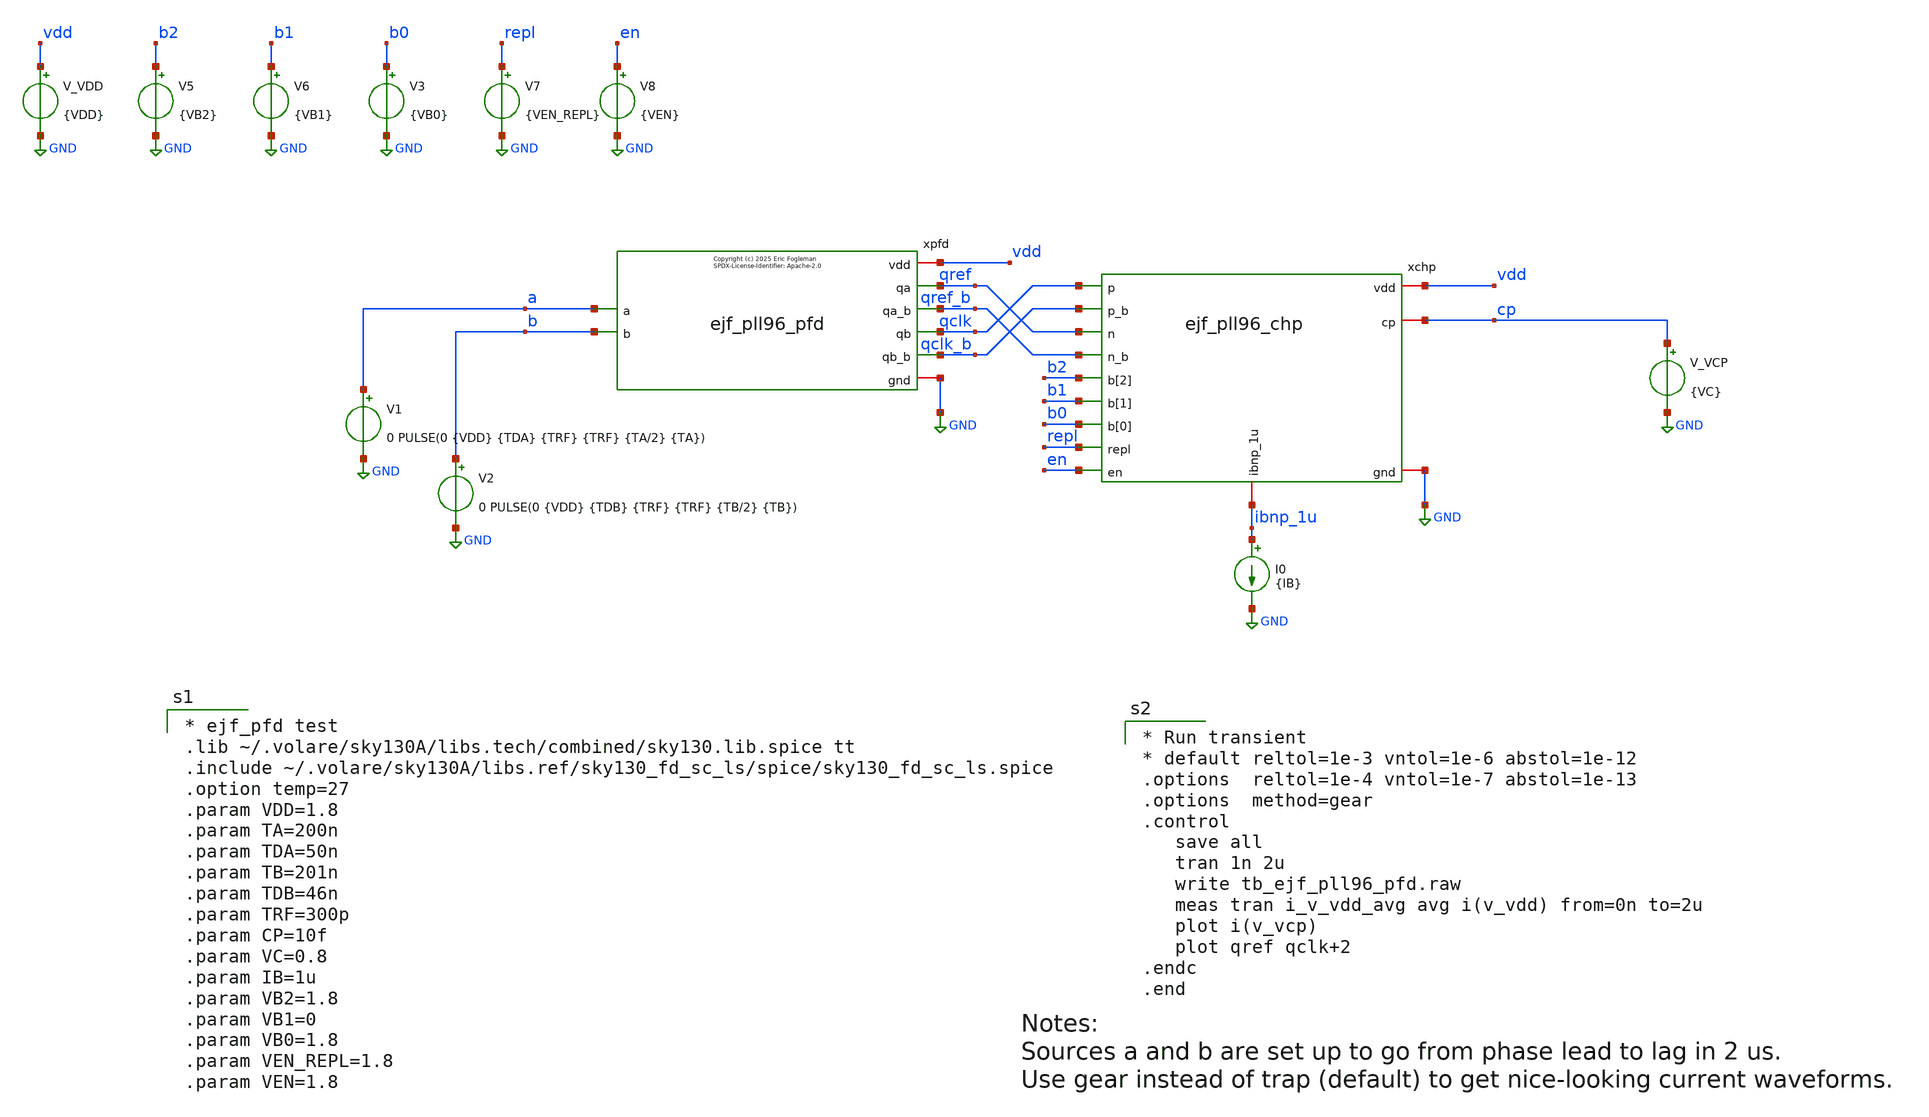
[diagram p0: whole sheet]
** sch_path: xschem/tb_ejf_pll96_pfd.sch
* xschem/ejf_pll96_dbuf.sym:
* Copyright (c) 2025 Eric Fogleman
**.subckt tb_ejf_pll96_pfd
V_VDD vdd GND {VDD}
.save i(v_vdd)
V1 a GND 0 PULSE(0 {VDD} {TDA} {TRF} {TRF} {TA/2} {TA})
xpfd qref a qclk b vdd GND qref_b qclk_b ejf_pll96_pfd
V2 b GND 0 PULSE(0 {VDD} {TDB} {TRF} {TRF} {TB/2} {TB})
xchp vdd qclk ibnp_1u qclk_b cp qref_b qref GND b1 repl en b2 b0 ejf_pll96_chp
I0 ibnp_1u GND {IB}
V_VCP cp GND {VC}
.save i(v_vcp)
V5 b2 GND {VB2}
.save i(v5)
V6 b1 GND {VB1}
.save i(v6)
V7 repl GND {VEN_REPL}
.save i(v7)
V8 en GND {VEN}
.save i(v8)
V3 b0 GND {VB0}
.save i(v3)
**** begin user architecture code

* ejf_pfd test
.lib ~/.volare/sky130A/libs.tech/combined/sky130.lib.spice tt
.include ~/.volare/sky130A/libs.ref/sky130_fd_sc_ls/spice/sky130_fd_sc_ls.spice
.option temp=27
.param VDD=1.8
.param TA=200n
.param TDA=50n
.param TB=201n
.param TDB=46n
.param TRF=300p
.param CP=10f
.param VC=0.8
.param IB=1u
.param VB2=1.8
.param VB1=0
.param VB0=1.8
.param VEN_REPL=1.8
.param VEN=1.8



* Run transient
* default reltol=1e-3 vntol=1e-6 abstol=1e-12
.options  reltol=1e-4 vntol=1e-7 abstol=1e-13
.options  method=gear
.control
   save all
   tran 1n 2u
   write tb_ejf_pll96_pfd.raw
   meas tran i_v_vdd_avg avg i(v_vdd) from=0n to=2u
   plot i(v_vcp)
   plot qref qclk+2
.endc
.end

**** end user architecture code
**.ends

* expanding   symbol:  ejf_pll96_pfd.sym # of pins=8
** sym_path: xschem/ejf_pll96_pfd.sym
** sch_path: xschem/ejf_pll96_pfd.sch
.subckt ejf_pll96_pfd qa a qb b vdd gnd qa_b qb_b
*.iopin vdd
*.iopin gnd
*.ipin a
*.ipin b
*.opin qa
*.opin qb
*.opin qa_b
*.opin qb_b
x3 a_b b_b gnd gnd vdd vdd y_par sky130_fd_sc_ls__nor2_2
x4 net1 gnd gnd vdd vdd rst_b sky130_fd_sc_ls__clkinv_1
x1 a vdd rst_b gnd gnd vdd vdd qa0 sky130_fd_sc_ls__dfrtp_2
x2 b vdd rst_b gnd gnd vdd vdd qb0 sky130_fd_sc_ls__dfrtp_2
x6 vdd qa0 qa_b qa gnd a_b ejf_pll96_diff_buf
x7 vdd qb0 qb_b qb gnd b_b ejf_pll96_diff_buf
x8 b_b a_b gnd gnd vdd vdd y_par sky130_fd_sc_ls__nor2_2
x10 y_par gnd gnd vdd vdd net2 sky130_fd_sc_ls__dlygate4sd3_1
x5 net2 gnd gnd vdd vdd net1 sky130_fd_sc_ls__dlygate4sd3_1
**** begin user architecture code

* Copyright (c) Eric Fogleman 2025
* SPDX-License-Identifier: Apache-2.0

**** end user architecture code
.ends


* expanding   symbol:  ejf_pll96_chp.sym # of pins=13
** sym_path: xschem/ejf_pll96_chp.sym
** sch_path: xschem/ejf_pll96_chp.sch
.subckt ejf_pll96_chp vdd p ibnp_1u p_b cp n_b n gnd b[1] repl en b[2] b[0]
*.iopin vdd
*.iopin gnd
*.iopin ibnp_1u
*.iopin cp
*.ipin p
*.ipin n_b
*.ipin p_b
*.ipin n
*.ipin en
*.ipin b[2],b[1],b[0]
*.ipin repl
XMP2_2 mp2d net12 vdd vdd sky130_fd_pr__pfet_01v8_lvt L=1.2 W=1.2 nf=2 ad='int((nf+1)/2) * W/nf * 0.29'
+ as='int((nf+2)/2) * W/nf * 0.29' pd='2*int((nf+1)/2) * (W/nf + 0.29)' ps='2*int((nf+2)/2) * (W/nf + 0.29)'
+ nrd='0.29 / W' nrs='0.29 / W' sa=0 sb=0 sd=0 mult=1 m=1
XMN2 net1 mn1g gnd gnd sky130_fd_pr__nfet_01v8 L=1.2 W=0.6 nf=1 ad='int((nf+1)/2) * W/nf * 0.29' as='int((nf+2)/2) * W/nf * 0.29'
+ pd='2*int((nf+1)/2) * (W/nf + 0.29)' ps='2*int((nf+2)/2) * (W/nf + 0.29)' nrd='0.29 / W' nrs='0.29 / W'
+ sa=0 sb=0 sd=0 mult=1 m=1
XMN2C mn1g mn1cg net1 gnd sky130_fd_pr__nfet_01v8 L=0.3 W=0.6 nf=1 ad='int((nf+1)/2) * W/nf * 0.29' as='int((nf+2)/2) * W/nf * 0.29'
+ pd='2*int((nf+1)/2) * (W/nf + 0.29)' ps='2*int((nf+2)/2) * (W/nf + 0.29)' nrd='0.29 / W' nrs='0.29 / W'
+ sa=0 sb=0 sd=0 mult=1 m=1
XMP1 mp1d mp1g vdd vdd sky130_fd_pr__pfet_01v8_lvt L=1.2 W=1.8 nf=3 ad='int((nf+1)/2) * W/nf * 0.29'
+ as='int((nf+2)/2) * W/nf * 0.29' pd='2*int((nf+1)/2) * (W/nf + 0.29)' ps='2*int((nf+2)/2) * (W/nf + 0.29)'
+ nrd='0.29 / W' nrs='0.29 / W' sa=0 sb=0 sd=0 mult=5 m=5
XMP2C mp1g ibnp_1u mp2d vdd sky130_fd_pr__pfet_01v8_lvt L=0.35 W=1.2 nf=1 ad='int((nf+1)/2) * W/nf * 0.29'
+ as='int((nf+2)/2) * W/nf * 0.29' pd='2*int((nf+1)/2) * (W/nf + 0.29)' ps='2*int((nf+2)/2) * (W/nf + 0.29)'
+ nrd='0.29 / W' nrs='0.29 / W' sa=0 sb=0 sd=0 mult=1 m=1
XMP1C mp1cd ibnp_1u mp1d vdd sky130_fd_pr__pfet_01v8_lvt L=0.35 W=1.2 nf=1 ad='int((nf+1)/2) * W/nf * 0.29'
+ as='int((nf+2)/2) * W/nf * 0.29' pd='2*int((nf+1)/2) * (W/nf + 0.29)' ps='2*int((nf+2)/2) * (W/nf + 0.29)'
+ nrd='0.29 / W' nrs='0.29 / W' sa=0 sb=0 sd=0 mult=5 m=5
XMN1 mn1d mn1g gnd gnd sky130_fd_pr__nfet_01v8 L=1.2 W=0.6 nf=1 ad='int((nf+1)/2) * W/nf * 0.29' as='int((nf+2)/2) * W/nf * 0.29'
+ pd='2*int((nf+1)/2) * (W/nf + 0.29)' ps='2*int((nf+2)/2) * (W/nf + 0.29)' nrd='0.29 / W' nrs='0.29 / W'
+ sa=0 sb=0 sd=0 mult=5 m=5
XM1C mn1cd mn1cg mn1d gnd sky130_fd_pr__nfet_01v8 L=0.3 W=0.6 nf=1 ad='int((nf+1)/2) * W/nf * 0.29' as='int((nf+2)/2) * W/nf * 0.29'
+ pd='2*int((nf+1)/2) * (W/nf + 0.29)' ps='2*int((nf+2)/2) * (W/nf + 0.29)' nrd='0.29 / W' nrs='0.29 / W'
+ sa=0 sb=0 sd=0 mult=5 m=5
XMP11 cp_repl p mp1cd vdd sky130_fd_pr__pfet_01v8 L=0.15 W=1 nf=1 ad='int((nf+1)/2) * W/nf * 0.29' as='int((nf+2)/2) * W/nf * 0.29'
+ pd='2*int((nf+1)/2) * (W/nf + 0.29)' ps='2*int((nf+2)/2) * (W/nf + 0.29)' nrd='0.29 / W' nrs='0.29 / W'
+ sa=0 sb=0 sd=0 mult=1 m=1
XMN11 cp_repl n_b mn1cd gnd sky130_fd_pr__nfet_01v8 L=0.15 W=1 nf=1 ad='int((nf+1)/2) * W/nf * 0.29'
+ as='int((nf+2)/2) * W/nf * 0.29' pd='2*int((nf+1)/2) * (W/nf + 0.29)' ps='2*int((nf+2)/2) * (W/nf + 0.29)'
+ nrd='0.29 / W' nrs='0.29 / W' sa=0 sb=0 sd=0 mult=1 m=1
XMP10 cp p_b mp1cd vdd sky130_fd_pr__pfet_01v8 L=0.15 W=1 nf=1 ad='int((nf+1)/2) * W/nf * 0.29' as='int((nf+2)/2) * W/nf * 0.29'
+ pd='2*int((nf+1)/2) * (W/nf + 0.29)' ps='2*int((nf+2)/2) * (W/nf + 0.29)' nrd='0.29 / W' nrs='0.29 / W'
+ sa=0 sb=0 sd=0 mult=1 m=1
XMN10 cp n mn1cd gnd sky130_fd_pr__nfet_01v8 L=0.15 W=1 nf=1 ad='int((nf+1)/2) * W/nf * 0.29' as='int((nf+2)/2) * W/nf * 0.29'
+ pd='2*int((nf+1)/2) * (W/nf + 0.29)' ps='2*int((nf+2)/2) * (W/nf + 0.29)' nrd='0.29 / W' nrs='0.29 / W'
+ sa=0 sb=0 sd=0 mult=1 m=1
XMN4CAP gnd mn1g gnd gnd sky130_fd_pr__nfet_01v8 L=1.2 W=0.6 nf=1 ad='int((nf+1)/2) * W/nf * 0.29' as='int((nf+2)/2) * W/nf * 0.29'
+ pd='2*int((nf+1)/2) * (W/nf + 0.29)' ps='2*int((nf+2)/2) * (W/nf + 0.29)' nrd='0.29 / W' nrs='0.29 / W'
+ sa=0 sb=0 sd=0 mult=11 m=11
XMP4CAP vdd mp1g vdd vdd sky130_fd_pr__pfet_01v8_lvt L=1.2 W=1.8 nf=3 ad='int((nf+1)/2) * W/nf * 0.29'
+ as='int((nf+2)/2) * W/nf * 0.29' pd='2*int((nf+1)/2) * (W/nf + 0.29)' ps='2*int((nf+2)/2) * (W/nf + 0.29)'
+ nrd='0.29 / W' nrs='0.29 / W' sa=0 sb=0 sd=0 mult=13 m=13
XMP5CAP vdd ibnp_1u vdd vdd sky130_fd_pr__pfet_01v8_lvt L=1.2 W=1.8 nf=3 ad='int((nf+1)/2) * W/nf * 0.29'
+ as='int((nf+2)/2) * W/nf * 0.29' pd='2*int((nf+1)/2) * (W/nf + 0.29)' ps='2*int((nf+2)/2) * (W/nf + 0.29)'
+ nrd='0.29 / W' nrs='0.29 / W' sa=0 sb=0 sd=0 mult=13 m=13
XMN5CAP gnd mn1cg gnd gnd sky130_fd_pr__nfet_01v8 L=1.2 W=0.6 nf=1 ad='int((nf+1)/2) * W/nf * 0.29' as='int((nf+2)/2) * W/nf * 0.29'
+ pd='2*int((nf+1)/2) * (W/nf + 0.29)' ps='2*int((nf+2)/2) * (W/nf + 0.29)' nrd='0.29 / W' nrs='0.29 / W'
+ sa=0 sb=0 sd=0 mult=11 m=11
XMP20 mp20d mp1g vdd vdd sky130_fd_pr__pfet_01v8_lvt L=1.2 W=1.8 nf=3 ad='int((nf+1)/2) * W/nf * 0.29'
+ as='int((nf+2)/2) * W/nf * 0.29' pd='2*int((nf+1)/2) * (W/nf + 0.29)' ps='2*int((nf+2)/2) * (W/nf + 0.29)'
+ nrd='0.29 / W' nrs='0.29 / W' sa=0 sb=0 sd=0 mult=5 m=5
XMN6 mp21cg mn1g gnd gnd sky130_fd_pr__nfet_01v8 L=1.2 W=0.6 nf=1 ad='int((nf+1)/2) * W/nf * 0.29' as='int((nf+2)/2) * W/nf * 0.29'
+ pd='2*int((nf+1)/2) * (W/nf + 0.29)' ps='2*int((nf+2)/2) * (W/nf + 0.29)' nrd='0.29 / W' nrs='0.29 / W'
+ sa=0 sb=0 sd=0 mult=1 m=1
XMPC1 vdd cp_repl vdd vdd sky130_fd_pr__pfet_01v8_lvt L=7.5 W=60 nf=10 ad='int((nf+1)/2) * W/nf * 0.29'
+ as='int((nf+2)/2) * W/nf * 0.29' pd='2*int((nf+1)/2) * (W/nf + 0.29)' ps='2*int((nf+2)/2) * (W/nf + 0.29)'
+ nrd='0.29 / W' nrs='0.29 / W' sa=0 sb=0 sd=0 mult=1 m=1
XM12 mn1cg en_b gnd gnd sky130_fd_pr__nfet_01v8 L=0.15 W=1 nf=1 ad='int((nf+1)/2) * W/nf * 0.29' as='int((nf+2)/2) * W/nf * 0.29'
+ pd='2*int((nf+1)/2) * (W/nf + 0.29)' ps='2*int((nf+2)/2) * (W/nf + 0.29)' nrd='0.29 / W' nrs='0.29 / W'
+ sa=0 sb=0 sd=0 mult=1 m=1
XM13 mn1g en_b gnd gnd sky130_fd_pr__nfet_01v8 L=0.15 W=1 nf=1 ad='int((nf+1)/2) * W/nf * 0.29' as='int((nf+2)/2) * W/nf * 0.29'
+ pd='2*int((nf+1)/2) * (W/nf + 0.29)' ps='2*int((nf+2)/2) * (W/nf + 0.29)' nrd='0.29 / W' nrs='0.29 / W'
+ sa=0 sb=0 sd=0 mult=1 m=1
XMP21P net3 amp_inp mp20d vdd sky130_fd_pr__pfet_01v8_lvt L=0.35 W=1.2 nf=1 ad='int((nf+1)/2) * W/nf * 0.29'
+ as='int((nf+2)/2) * W/nf * 0.29' pd='2*int((nf+1)/2) * (W/nf + 0.29)' ps='2*int((nf+2)/2) * (W/nf + 0.29)'
+ nrd='0.29 / W' nrs='0.29 / W' sa=0 sb=0 sd=0 mult=1 m=1
XMP21N net4 cp_repl mp20d vdd sky130_fd_pr__pfet_01v8_lvt L=0.35 W=1.2 nf=1 ad='int((nf+1)/2) * W/nf * 0.29'
+ as='int((nf+2)/2) * W/nf * 0.29' pd='2*int((nf+1)/2) * (W/nf + 0.29)' ps='2*int((nf+2)/2) * (W/nf + 0.29)'
+ nrd='0.29 / W' nrs='0.29 / W' sa=0 sb=0 sd=0 mult=1 m=1
XMP24 mp21cg mp21cg mp20d vdd sky130_fd_pr__pfet_01v8_lvt L=2.8 W=1.2 nf=1 ad='int((nf+1)/2) * W/nf * 0.29'
+ as='int((nf+2)/2) * W/nf * 0.29' pd='2*int((nf+1)/2) * (W/nf + 0.29)' ps='2*int((nf+2)/2) * (W/nf + 0.29)'
+ nrd='0.29 / W' nrs='0.29 / W' sa=0 sb=0 sd=0 mult=1 m=1
XMP21NC cp_repl mp21cg net4 vdd sky130_fd_pr__pfet_01v8_lvt L=0.35 W=1.2 nf=1 ad='int((nf+1)/2) * W/nf * 0.29'
+ as='int((nf+2)/2) * W/nf * 0.29' pd='2*int((nf+1)/2) * (W/nf + 0.29)' ps='2*int((nf+2)/2) * (W/nf + 0.29)'
+ nrd='0.29 / W' nrs='0.29 / W' sa=0 sb=0 sd=0 mult=1 m=1
XMP21PC net2 mp21cg net3 vdd sky130_fd_pr__pfet_01v8_lvt L=0.35 W=1.2 nf=1 ad='int((nf+1)/2) * W/nf * 0.29'
+ as='int((nf+2)/2) * W/nf * 0.29' pd='2*int((nf+1)/2) * (W/nf + 0.29)' ps='2*int((nf+2)/2) * (W/nf + 0.29)'
+ nrd='0.29 / W' nrs='0.29 / W' sa=0 sb=0 sd=0 mult=1 m=1
XMN24 net6 net2 gnd gnd sky130_fd_pr__nfet_01v8 L=1.2 W=0.6 nf=1 ad='int((nf+1)/2) * W/nf * 0.29' as='int((nf+2)/2) * W/nf * 0.29'
+ pd='2*int((nf+1)/2) * (W/nf + 0.29)' ps='2*int((nf+2)/2) * (W/nf + 0.29)' nrd='0.29 / W' nrs='0.29 / W'
+ sa=0 sb=0 sd=0 mult=2 m=2
XMN23 net5 net2 gnd gnd sky130_fd_pr__nfet_01v8 L=1.2 W=0.6 nf=1 ad='int((nf+1)/2) * W/nf * 0.29' as='int((nf+2)/2) * W/nf * 0.29'
+ pd='2*int((nf+1)/2) * (W/nf + 0.29)' ps='2*int((nf+2)/2) * (W/nf + 0.29)' nrd='0.29 / W' nrs='0.29 / W'
+ sa=0 sb=0 sd=0 mult=2 m=2
XMN24C net2 mn1cg net6 gnd sky130_fd_pr__nfet_01v8 L=0.3 W=0.6 nf=1 ad='int((nf+1)/2) * W/nf * 0.29'
+ as='int((nf+2)/2) * W/nf * 0.29' pd='2*int((nf+1)/2) * (W/nf + 0.29)' ps='2*int((nf+2)/2) * (W/nf + 0.29)'
+ nrd='0.29 / W' nrs='0.29 / W' sa=0 sb=0 sd=0 mult=2 m=2
XMN23C cp_repl mn1cg net5 gnd sky130_fd_pr__nfet_01v8 L=0.3 W=0.6 nf=1 ad='int((nf+1)/2) * W/nf * 0.29'
+ as='int((nf+2)/2) * W/nf * 0.29' pd='2*int((nf+1)/2) * (W/nf + 0.29)' ps='2*int((nf+2)/2) * (W/nf + 0.29)'
+ nrd='0.29 / W' nrs='0.29 / W' sa=0 sb=0 sd=0 mult=2 m=2
XM8 net9 repl_b gnd gnd sky130_fd_pr__nfet_01v8 L=0.15 W=1 nf=1 ad='int((nf+1)/2) * W/nf * 0.29' as='int((nf+2)/2) * W/nf * 0.29'
+ pd='2*int((nf+1)/2) * (W/nf + 0.29)' ps='2*int((nf+2)/2) * (W/nf + 0.29)' nrd='0.29 / W' nrs='0.29 / W'
+ sa=0 sb=0 sd=0 mult=1 m=1
XM5 net7 repl_bb vdd vdd sky130_fd_pr__pfet_01v8_hvt L=0.15 W=2 nf=1 ad='int((nf+1)/2) * W/nf * 0.29'
+ as='int((nf+2)/2) * W/nf * 0.29' pd='2*int((nf+1)/2) * (W/nf + 0.29)' ps='2*int((nf+2)/2) * (W/nf + 0.29)'
+ nrd='0.29 / W' nrs='0.29 / W' sa=0 sb=0 sd=0 mult=1 m=1
XM6 amp_inp net7 net7 net7 sky130_fd_pr__pfet_01v8_lvt L=0.35 W=40 nf=8 ad='int((nf+1)/2) * W/nf * 0.29'
+ as='int((nf+2)/2) * W/nf * 0.29' pd='2*int((nf+1)/2) * (W/nf + 0.29)' ps='2*int((nf+2)/2) * (W/nf + 0.29)'
+ nrd='0.29 / W' nrs='0.29 / W' sa=0 sb=0 sd=0 mult=1 m=1
XM7 net9 amp_inp amp_inp amp_inp sky130_fd_pr__pfet_01v8_lvt L=0.35 W=40 nf=8 ad='int((nf+1)/2) * W/nf * 0.29'
+ as='int((nf+2)/2) * W/nf * 0.29' pd='2*int((nf+1)/2) * (W/nf + 0.29)' ps='2*int((nf+2)/2) * (W/nf + 0.29)'
+ nrd='0.29 / W' nrs='0.29 / W' sa=0 sb=0 sd=0 mult=1 m=1
XMN4 net8 repl_bb amp_inp gnd sky130_fd_pr__nfet_01v8 L=0.15 W=1 nf=1 ad='int((nf+1)/2) * W/nf * 0.29'
+ as='int((nf+2)/2) * W/nf * 0.29' pd='2*int((nf+1)/2) * (W/nf + 0.29)' ps='2*int((nf+2)/2) * (W/nf + 0.29)'
+ nrd='0.29 / W' nrs='0.29 / W' sa=0 sb=0 sd=0 mult=1 m=1
XM9 net8 repl_b amp_inp vdd sky130_fd_pr__pfet_01v8_hvt L=0.15 W=2 nf=1 ad='int((nf+1)/2) * W/nf * 0.29'
+ as='int((nf+2)/2) * W/nf * 0.29' pd='2*int((nf+1)/2) * (W/nf + 0.29)' ps='2*int((nf+2)/2) * (W/nf + 0.29)'
+ nrd='0.29 / W' nrs='0.29 / W' sa=0 sb=0 sd=0 mult=1 m=1
XMP2_1 mp2d net10 vdd vdd sky130_fd_pr__pfet_01v8_lvt L=1.2 W=0.6 nf=1 ad='int((nf+1)/2) * W/nf * 0.29'
+ as='int((nf+2)/2) * W/nf * 0.29' pd='2*int((nf+1)/2) * (W/nf + 0.29)' ps='2*int((nf+2)/2) * (W/nf + 0.29)'
+ nrd='0.29 / W' nrs='0.29 / W' sa=0 sb=0 sd=0 mult=1 m=1
XMP2_1P5 mp2d net11 vdd vdd sky130_fd_pr__pfet_01v8_lvt L=1.2 W=0.9 nf=1 ad='int((nf+1)/2) * W/nf * 0.29'
+ as='int((nf+2)/2) * W/nf * 0.29' pd='2*int((nf+1)/2) * (W/nf + 0.29)' ps='2*int((nf+2)/2) * (W/nf + 0.29)'
+ nrd='0.29 / W' nrs='0.29 / W' sa=0 sb=0 sd=0 mult=1 m=1
XM4 net11 b_bb[1] vdd vdd sky130_fd_pr__pfet_01v8_hvt L=0.15 W=2 nf=1 ad='int((nf+1)/2) * W/nf * 0.29'
+ as='int((nf+2)/2) * W/nf * 0.29' pd='2*int((nf+1)/2) * (W/nf + 0.29)' ps='2*int((nf+2)/2) * (W/nf + 0.29)'
+ nrd='0.29 / W' nrs='0.29 / W' sa=0 sb=0 sd=0 mult=1 m=1
XMP3C mn1cg ibnp_1u net13 vdd sky130_fd_pr__pfet_01v8_lvt L=0.35 W=1.2 nf=1 ad='int((nf+1)/2) * W/nf * 0.29'
+ as='int((nf+2)/2) * W/nf * 0.29' pd='2*int((nf+1)/2) * (W/nf + 0.29)' ps='2*int((nf+2)/2) * (W/nf + 0.29)'
+ nrd='0.29 / W' nrs='0.29 / W' sa=0 sb=0 sd=0 mult=1 m=1
XMP3 net13 mp1g vdd vdd sky130_fd_pr__pfet_01v8_lvt L=1.2 W=1.8 nf=3 ad='int((nf+1)/2) * W/nf * 0.29'
+ as='int((nf+2)/2) * W/nf * 0.29' pd='2*int((nf+1)/2) * (W/nf + 0.29)' ps='2*int((nf+2)/2) * (W/nf + 0.29)'
+ nrd='0.29 / W' nrs='0.29 / W' sa=0 sb=0 sd=0 mult=1 m=1
x1 vdd en en_bb en_b gnd ejf_pll96_dbuf
x2 vdd repl repl_bb repl_b gnd ejf_pll96_dbuf
x3[2] vdd b[2] b_bb[2] b_b[2] gnd ejf_pll96_dbuf
x3[1] vdd b[1] b_bb[1] b_b[1] gnd ejf_pll96_dbuf
x3[0] vdd b[0] b_bb[0] b_b[0] gnd ejf_pll96_dbuf
XM1 mp1g b_b[1] net11 vdd sky130_fd_pr__pfet_01v8_hvt L=0.15 W=2 nf=1 ad='int((nf+1)/2) * W/nf * 0.29'
+ as='int((nf+2)/2) * W/nf * 0.29' pd='2*int((nf+1)/2) * (W/nf + 0.29)' ps='2*int((nf+2)/2) * (W/nf + 0.29)'
+ nrd='0.29 / W' nrs='0.29 / W' sa=0 sb=0 sd=0 mult=1 m=1
XM2 net10 b_bb[0] vdd vdd sky130_fd_pr__pfet_01v8_hvt L=0.15 W=2 nf=1 ad='int((nf+1)/2) * W/nf * 0.29'
+ as='int((nf+2)/2) * W/nf * 0.29' pd='2*int((nf+1)/2) * (W/nf + 0.29)' ps='2*int((nf+2)/2) * (W/nf + 0.29)'
+ nrd='0.29 / W' nrs='0.29 / W' sa=0 sb=0 sd=0 mult=1 m=1
XM3 mp1g b_b[0] net10 vdd sky130_fd_pr__pfet_01v8_hvt L=0.15 W=2 nf=1 ad='int((nf+1)/2) * W/nf * 0.29'
+ as='int((nf+2)/2) * W/nf * 0.29' pd='2*int((nf+1)/2) * (W/nf + 0.29)' ps='2*int((nf+2)/2) * (W/nf + 0.29)'
+ nrd='0.29 / W' nrs='0.29 / W' sa=0 sb=0 sd=0 mult=1 m=1
XM10 ibnp_1u en_bb vdd vdd sky130_fd_pr__pfet_01v8_hvt L=0.15 W=2 nf=1 ad='int((nf+1)/2) * W/nf * 0.29'
+ as='int((nf+2)/2) * W/nf * 0.29' pd='2*int((nf+1)/2) * (W/nf + 0.29)' ps='2*int((nf+2)/2) * (W/nf + 0.29)'
+ nrd='0.29 / W' nrs='0.29 / W' sa=0 sb=0 sd=0 mult=1 m=1
XM11 mp1g en_bb vdd vdd sky130_fd_pr__pfet_01v8_hvt L=0.15 W=2 nf=1 ad='int((nf+1)/2) * W/nf * 0.29'
+ as='int((nf+2)/2) * W/nf * 0.29' pd='2*int((nf+1)/2) * (W/nf + 0.29)' ps='2*int((nf+2)/2) * (W/nf + 0.29)'
+ nrd='0.29 / W' nrs='0.29 / W' sa=0 sb=0 sd=0 mult=1 m=1
XR1 net16 net17 vdd sky130_fd_pr__res_high_po_0p35 L=23 mult=1 m=1
XR2 ibnp_1u net16 vdd sky130_fd_pr__res_high_po_0p35 L=23 mult=1 m=1
XR3 net15 mp1g vdd sky130_fd_pr__res_high_po_0p35 L=23 mult=1 m=1
XR4 net17 net15 vdd sky130_fd_pr__res_high_po_0p35 L=23 mult=1 m=1
XR5[1] vdd vdd vdd sky130_fd_pr__res_high_po_0p35 L=23 mult=1 m=1
XR5[0] vdd vdd vdd sky130_fd_pr__res_high_po_0p35 L=23 mult=1 m=1
XR5 net14 net19 gnd sky130_fd_pr__res_high_po_0p35 L=23 mult=1 m=1
XR6 net20 net14 gnd sky130_fd_pr__res_high_po_0p35 L=23 mult=1 m=1
XR7 net21 net20 gnd sky130_fd_pr__res_high_po_0p35 L=23 mult=1 m=1
XR8 mn1g net21 gnd sky130_fd_pr__res_high_po_0p35 L=23 mult=1 m=1
XR9 net18 mn1cg gnd sky130_fd_pr__res_high_po_0p35 L=23 mult=1 m=1
XR10 net22 net18 gnd sky130_fd_pr__res_high_po_0p35 L=23 mult=1 m=1
XR11 net23 net22 gnd sky130_fd_pr__res_high_po_0p35 L=23 mult=1 m=1
XR12 net19 net23 gnd sky130_fd_pr__res_high_po_0p35 L=23 mult=1 m=1
XR13[1] gnd gnd gnd sky130_fd_pr__res_high_po_0p35 L=23 mult=1 m=1
XR13[0] gnd gnd gnd sky130_fd_pr__res_high_po_0p35 L=23 mult=1 m=1
XR13 net24 net8 vdd sky130_fd_pr__res_high_po_0p35 L=23 mult=1 m=1
XR14 cp net24 vdd sky130_fd_pr__res_high_po_0p35 L=23 mult=1 m=1
XR15[1] vdd vdd vdd sky130_fd_pr__res_high_po_0p35 L=23 mult=1 m=1
XR15[0] vdd vdd vdd sky130_fd_pr__res_high_po_0p35 L=23 mult=1 m=1
XM14 net12 b_bb[2] vdd vdd sky130_fd_pr__pfet_01v8_hvt L=0.15 W=2 nf=1 ad='int((nf+1)/2) * W/nf * 0.29'
+ as='int((nf+2)/2) * W/nf * 0.29' pd='2*int((nf+1)/2) * (W/nf + 0.29)' ps='2*int((nf+2)/2) * (W/nf + 0.29)'
+ nrd='0.29 / W' nrs='0.29 / W' sa=0 sb=0 sd=0 mult=1 m=1
XM15 mp1g b_b[2] net12 vdd sky130_fd_pr__pfet_01v8_hvt L=0.15 W=2 nf=1 ad='int((nf+1)/2) * W/nf * 0.29'
+ as='int((nf+2)/2) * W/nf * 0.29' pd='2*int((nf+1)/2) * (W/nf + 0.29)' ps='2*int((nf+2)/2) * (W/nf + 0.29)'
+ nrd='0.29 / W' nrs='0.29 / W' sa=0 sb=0 sd=0 mult=1 m=1
.ends


* expanding   symbol:  ejf_pll96_diff_buf.sym # of pins=6
** sym_path: xschem/ejf_pll96_diff_buf.sym
** sch_path: xschem/ejf_pll96_diff_buf.sch
.subckt ejf_pll96_diff_buf vdd a y_b y gnd a_b
*.iopin vdd
*.iopin gnd
*.ipin a
*.opin y_b
*.opin y
*.opin a_b
XM11 a_b a gnd gnd sky130_fd_pr__nfet_01v8 L=0.15 W=0.84 nf=2 ad='int((nf+1)/2) * W/nf * 0.29' as='int((nf+2)/2) * W/nf * 0.29'
+ pd='2*int((nf+1)/2) * (W/nf + 0.29)' ps='2*int((nf+2)/2) * (W/nf + 0.29)' nrd='0.29 / W' nrs='0.29 / W'
+ sa=0 sb=0 sd=0 mult=1 m=1
XM12 a_b a vdd vdd sky130_fd_pr__pfet_01v8_hvt L=0.15 W=3.36 nf=3 ad='int((nf+1)/2) * W/nf * 0.29' as='int((nf+2)/2) * W/nf * 0.29'
+ pd='2*int((nf+1)/2) * (W/nf + 0.29)' ps='2*int((nf+2)/2) * (W/nf + 0.29)' nrd='0.29 / W' nrs='0.29 / W'
+ sa=0 sb=0 sd=0 mult=1 m=1
XM1 y_b net1 gnd gnd sky130_fd_pr__nfet_01v8 L=0.15 W=0.84 nf=2 ad='int((nf+1)/2) * W/nf * 0.29' as='int((nf+2)/2) * W/nf * 0.29'
+ pd='2*int((nf+1)/2) * (W/nf + 0.29)' ps='2*int((nf+2)/2) * (W/nf + 0.29)' nrd='0.29 / W' nrs='0.29 / W'
+ sa=0 sb=0 sd=0 mult=1 m=1
XM2 y_b net1 vdd vdd sky130_fd_pr__pfet_01v8_hvt L=0.15 W=3.36 nf=3 ad='int((nf+1)/2) * W/nf * 0.29'
+ as='int((nf+2)/2) * W/nf * 0.29' pd='2*int((nf+1)/2) * (W/nf + 0.29)' ps='2*int((nf+2)/2) * (W/nf + 0.29)'
+ nrd='0.29 / W' nrs='0.29 / W' sa=0 sb=0 sd=0 mult=1 m=1
XM3 net1 a_b gnd gnd sky130_fd_pr__nfet_01v8 L=0.15 W=0.84 nf=2 ad='int((nf+1)/2) * W/nf * 0.29' as='int((nf+2)/2) * W/nf * 0.29'
+ pd='2*int((nf+1)/2) * (W/nf + 0.29)' ps='2*int((nf+2)/2) * (W/nf + 0.29)' nrd='0.29 / W' nrs='0.29 / W'
+ sa=0 sb=0 sd=0 mult=1 m=1
XM4 net1 a_b vdd vdd sky130_fd_pr__pfet_01v8_hvt L=0.15 W=3.36 nf=3 ad='int((nf+1)/2) * W/nf * 0.29'
+ as='int((nf+2)/2) * W/nf * 0.29' pd='2*int((nf+1)/2) * (W/nf + 0.29)' ps='2*int((nf+2)/2) * (W/nf + 0.29)'
+ nrd='0.29 / W' nrs='0.29 / W' sa=0 sb=0 sd=0 mult=1 m=1
XM5 y net2 gnd gnd sky130_fd_pr__nfet_01v8 L=0.15 W=0.84 nf=2 ad='int((nf+1)/2) * W/nf * 0.29' as='int((nf+2)/2) * W/nf * 0.29'
+ pd='2*int((nf+1)/2) * (W/nf + 0.29)' ps='2*int((nf+2)/2) * (W/nf + 0.29)' nrd='0.29 / W' nrs='0.29 / W'
+ sa=0 sb=0 sd=0 mult=1 m=1
XM6 y net2 vdd vdd sky130_fd_pr__pfet_01v8_hvt L=0.15 W=3.36 nf=3 ad='int((nf+1)/2) * W/nf * 0.29' as='int((nf+2)/2) * W/nf * 0.29'
+ pd='2*int((nf+1)/2) * (W/nf + 0.29)' ps='2*int((nf+2)/2) * (W/nf + 0.29)' nrd='0.29 / W' nrs='0.29 / W'
+ sa=0 sb=0 sd=0 mult=1 m=1
XM9 net2 gnd a_b VDD sky130_fd_pr__pfet_01v8_hvt L=0.15 W=3.36 nf=3 ad='int((nf+1)/2) * W/nf * 0.29'
+ as='int((nf+2)/2) * W/nf * 0.29' pd='2*int((nf+1)/2) * (W/nf + 0.29)' ps='2*int((nf+2)/2) * (W/nf + 0.29)'
+ nrd='0.29 / W' nrs='0.29 / W' sa=0 sb=0 sd=0 mult=1 m=1
XM10 net2 vdd a_b GND sky130_fd_pr__nfet_01v8 L=0.15 W=0.84 nf=2 ad='int((nf+1)/2) * W/nf * 0.29' as='int((nf+2)/2) * W/nf * 0.29'
+ pd='2*int((nf+1)/2) * (W/nf + 0.29)' ps='2*int((nf+2)/2) * (W/nf + 0.29)' nrd='0.29 / W' nrs='0.29 / W'
+ sa=0 sb=0 sd=0 mult=1 m=1
**** begin user architecture code

* Copyright (c) Eric Fogleman 2025
* SPDX-License-Identifier: Apache-2.0

**** end user architecture code
.ends


* expanding   symbol:  ejf_pll96_dbuf.sym # of pins=5
** sym_path: xschem/ejf_pll96_dbuf.sym
** sch_path: xschem/ejf_pll96_dbuf.sch
.subckt ejf_pll96_dbuf vdd a y y_b gnd
*.ipin a
*.iopin vdd
*.iopin gnd
*.opin y
*.opin y_b
XMP1 y_b a vdd vdd sky130_fd_pr__pfet_01v8_hvt L=0.15 W=2 nf=1 ad='int((nf+1)/2) * W/nf * 0.29' as='int((nf+2)/2) * W/nf * 0.29'
+ pd='2*int((nf+1)/2) * (W/nf + 0.29)' ps='2*int((nf+2)/2) * (W/nf + 0.29)' nrd='0.29 / W' nrs='0.29 / W'
+ sa=0 sb=0 sd=0 mult=1 m=1
XMP3 y y_b vdd vdd sky130_fd_pr__pfet_01v8_hvt L=0.15 W=2 nf=1 ad='int((nf+1)/2) * W/nf * 0.29' as='int((nf+2)/2) * W/nf * 0.29'
+ pd='2*int((nf+1)/2) * (W/nf + 0.29)' ps='2*int((nf+2)/2) * (W/nf + 0.29)' nrd='0.29 / W' nrs='0.29 / W'
+ sa=0 sb=0 sd=0 mult=1 m=1
XMN4 y y_b gnd gnd sky130_fd_pr__nfet_01v8 L=0.15 W=1 nf=1 ad='int((nf+1)/2) * W/nf * 0.29' as='int((nf+2)/2) * W/nf * 0.29'
+ pd='2*int((nf+1)/2) * (W/nf + 0.29)' ps='2*int((nf+2)/2) * (W/nf + 0.29)' nrd='0.29 / W' nrs='0.29 / W'
+ sa=0 sb=0 sd=0 mult=1 m=1
XMN2 y_b a gnd gnd sky130_fd_pr__nfet_01v8 L=0.15 W=1 nf=1 ad='int((nf+1)/2) * W/nf * 0.29' as='int((nf+2)/2) * W/nf * 0.29'
+ pd='2*int((nf+1)/2) * (W/nf + 0.29)' ps='2*int((nf+2)/2) * (W/nf + 0.29)' nrd='0.29 / W' nrs='0.29 / W'
+ sa=0 sb=0 sd=0 mult=1 m=1
**** begin user architecture code

* Copyright (c) Eric Fogleman 2025
* SPDX-License-Identifier: Apache-2.0

**** end user architecture code
.ends

.GLOBAL GND
.end
